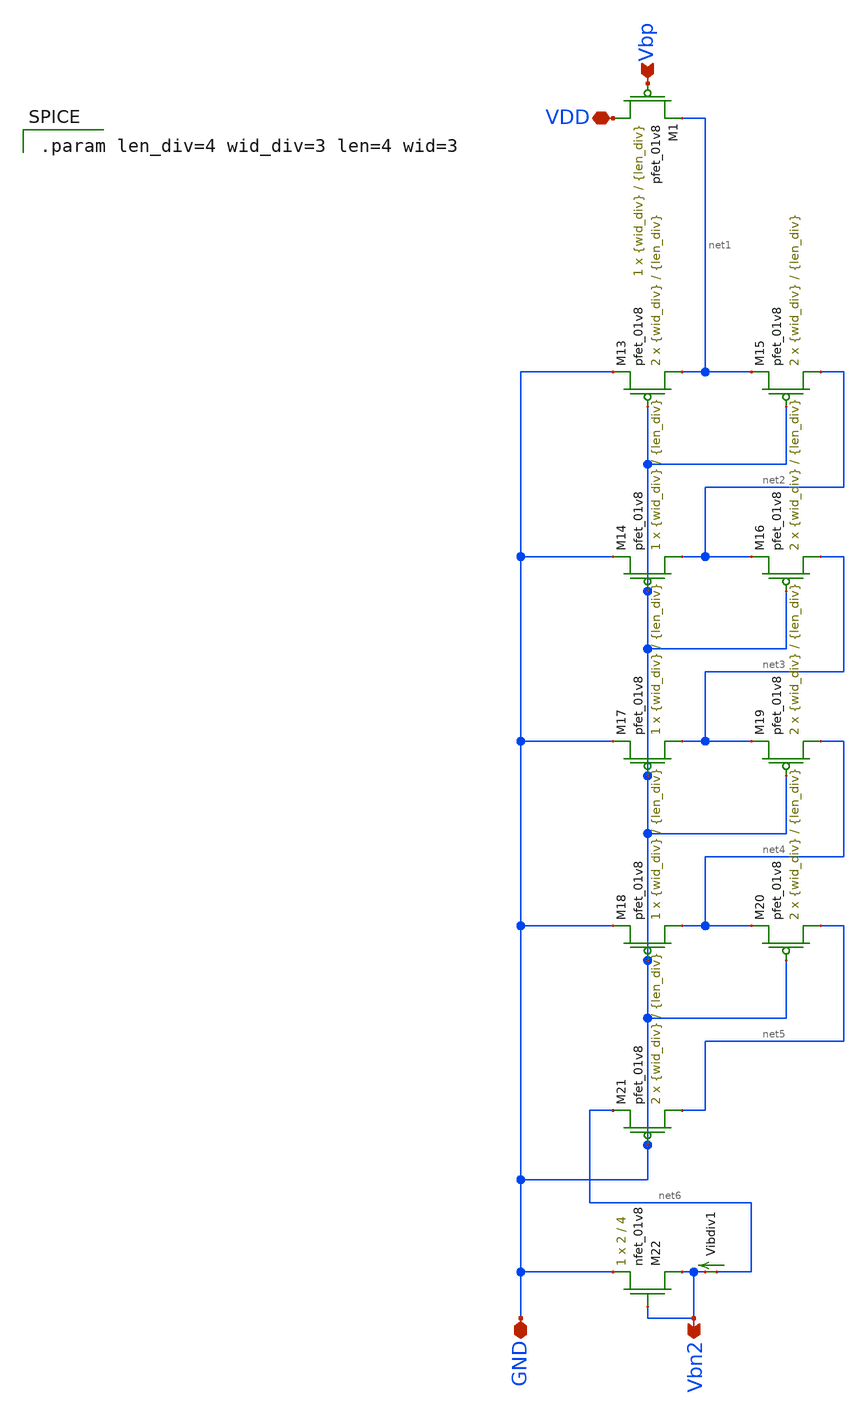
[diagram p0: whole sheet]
** sch_path: mp3/current_divider_lds.sch
**.subckt current_divider_lds GND Vbn2 Vbp VDD
*.iopin GND
*.opin Vbn2
*.ipin Vbp
*.iopin VDD
XM1 VDD Vbp net1 VDD sky130_fd_pr__pfet_01v8 L={len_div} W={wid_div} nf=1 ad='int((nf+1)/2) * W/nf * 0.29'
+ as='int((nf+2)/2) * W/nf * 0.29' pd='2*int((nf+1)/2) * (W/nf + 0.29)' ps='2*int((nf+2)/2) * (W/nf + 0.29)'
+ nrd='0.29 / W' nrs='0.29 / W' sa=0 sb=0 sd=0 mult=1 m=1
XM13 net1 GND GND VDD sky130_fd_pr__pfet_01v8 L={len_div} W={wid_div} nf=1 ad='int((nf+1)/2) * W/nf * 0.29'
+ as='int((nf+2)/2) * W/nf * 0.29' pd='2*int((nf+1)/2) * (W/nf + 0.29)' ps='2*int((nf+2)/2) * (W/nf + 0.29)'
+ nrd='0.29 / W' nrs='0.29 / W' sa=0 sb=0 sd=0 mult=2 m=2
XM14 net2 GND GND VDD sky130_fd_pr__pfet_01v8 L={len_div} W={wid_div} nf=1 ad='int((nf+1)/2) * W/nf * 0.29'
+ as='int((nf+2)/2) * W/nf * 0.29' pd='2*int((nf+1)/2) * (W/nf + 0.29)' ps='2*int((nf+2)/2) * (W/nf + 0.29)'
+ nrd='0.29 / W' nrs='0.29 / W' sa=0 sb=0 sd=0 mult=1 m=1
XM15 net2 GND net1 VDD sky130_fd_pr__pfet_01v8 L={len_div} W={wid_div} nf=1 ad='int((nf+1)/2) * W/nf * 0.29'
+ as='int((nf+2)/2) * W/nf * 0.29' pd='2*int((nf+1)/2) * (W/nf + 0.29)' ps='2*int((nf+2)/2) * (W/nf + 0.29)'
+ nrd='0.29 / W' nrs='0.29 / W' sa=0 sb=0 sd=0 mult=2 m=2
XM16 net3 GND net2 VDD sky130_fd_pr__pfet_01v8 L={len_div} W={wid_div} nf=1 ad='int((nf+1)/2) * W/nf * 0.29'
+ as='int((nf+2)/2) * W/nf * 0.29' pd='2*int((nf+1)/2) * (W/nf + 0.29)' ps='2*int((nf+2)/2) * (W/nf + 0.29)'
+ nrd='0.29 / W' nrs='0.29 / W' sa=0 sb=0 sd=0 mult=2 m=2
XM17 net3 GND GND VDD sky130_fd_pr__pfet_01v8 L={len_div} W={wid_div} nf=1 ad='int((nf+1)/2) * W/nf * 0.29'
+ as='int((nf+2)/2) * W/nf * 0.29' pd='2*int((nf+1)/2) * (W/nf + 0.29)' ps='2*int((nf+2)/2) * (W/nf + 0.29)'
+ nrd='0.29 / W' nrs='0.29 / W' sa=0 sb=0 sd=0 mult=1 m=1
XM18 net4 GND GND VDD sky130_fd_pr__pfet_01v8 L={len_div} W={wid_div} nf=1 ad='int((nf+1)/2) * W/nf * 0.29'
+ as='int((nf+2)/2) * W/nf * 0.29' pd='2*int((nf+1)/2) * (W/nf + 0.29)' ps='2*int((nf+2)/2) * (W/nf + 0.29)'
+ nrd='0.29 / W' nrs='0.29 / W' sa=0 sb=0 sd=0 mult=1 m=1
XM19 net4 GND net3 VDD sky130_fd_pr__pfet_01v8 L={len_div} W={wid_div} nf=1 ad='int((nf+1)/2) * W/nf * 0.29'
+ as='int((nf+2)/2) * W/nf * 0.29' pd='2*int((nf+1)/2) * (W/nf + 0.29)' ps='2*int((nf+2)/2) * (W/nf + 0.29)'
+ nrd='0.29 / W' nrs='0.29 / W' sa=0 sb=0 sd=0 mult=2 m=2
XM20 net5 GND net4 VDD sky130_fd_pr__pfet_01v8 L={len_div} W={wid_div} nf=1 ad='int((nf+1)/2) * W/nf * 0.29'
+ as='int((nf+2)/2) * W/nf * 0.29' pd='2*int((nf+1)/2) * (W/nf + 0.29)' ps='2*int((nf+2)/2) * (W/nf + 0.29)'
+ nrd='0.29 / W' nrs='0.29 / W' sa=0 sb=0 sd=0 mult=2 m=2
XM21 net5 GND net6 VDD sky130_fd_pr__pfet_01v8 L={len_div} W={wid_div} nf=1 ad='int((nf+1)/2) * W/nf * 0.29'
+ as='int((nf+2)/2) * W/nf * 0.29' pd='2*int((nf+1)/2) * (W/nf + 0.29)' ps='2*int((nf+2)/2) * (W/nf + 0.29)'
+ nrd='0.29 / W' nrs='0.29 / W' sa=0 sb=0 sd=0 mult=2 m=2
XM22 Vbn2 Vbn2 GND GND sky130_fd_pr__nfet_01v8 L=4 W=2 nf=1 ad='int((nf+1)/2) * W/nf * 0.29' as='int((nf+2)/2) * W/nf * 0.29'
+ pd='2*int((nf+1)/2) * (W/nf + 0.29)' ps='2*int((nf+2)/2) * (W/nf + 0.29)' nrd='0.29 / W' nrs='0.29 / W'
+ sa=0 sb=0 sd=0 mult=1 m=1
Vibdiv1 net6 Vbn2 0
.save i(vibdiv1)
**** begin user architecture code

.param len_div=4 wid_div=3 len=4 wid=3

**** end user architecture code
**.ends
.end
